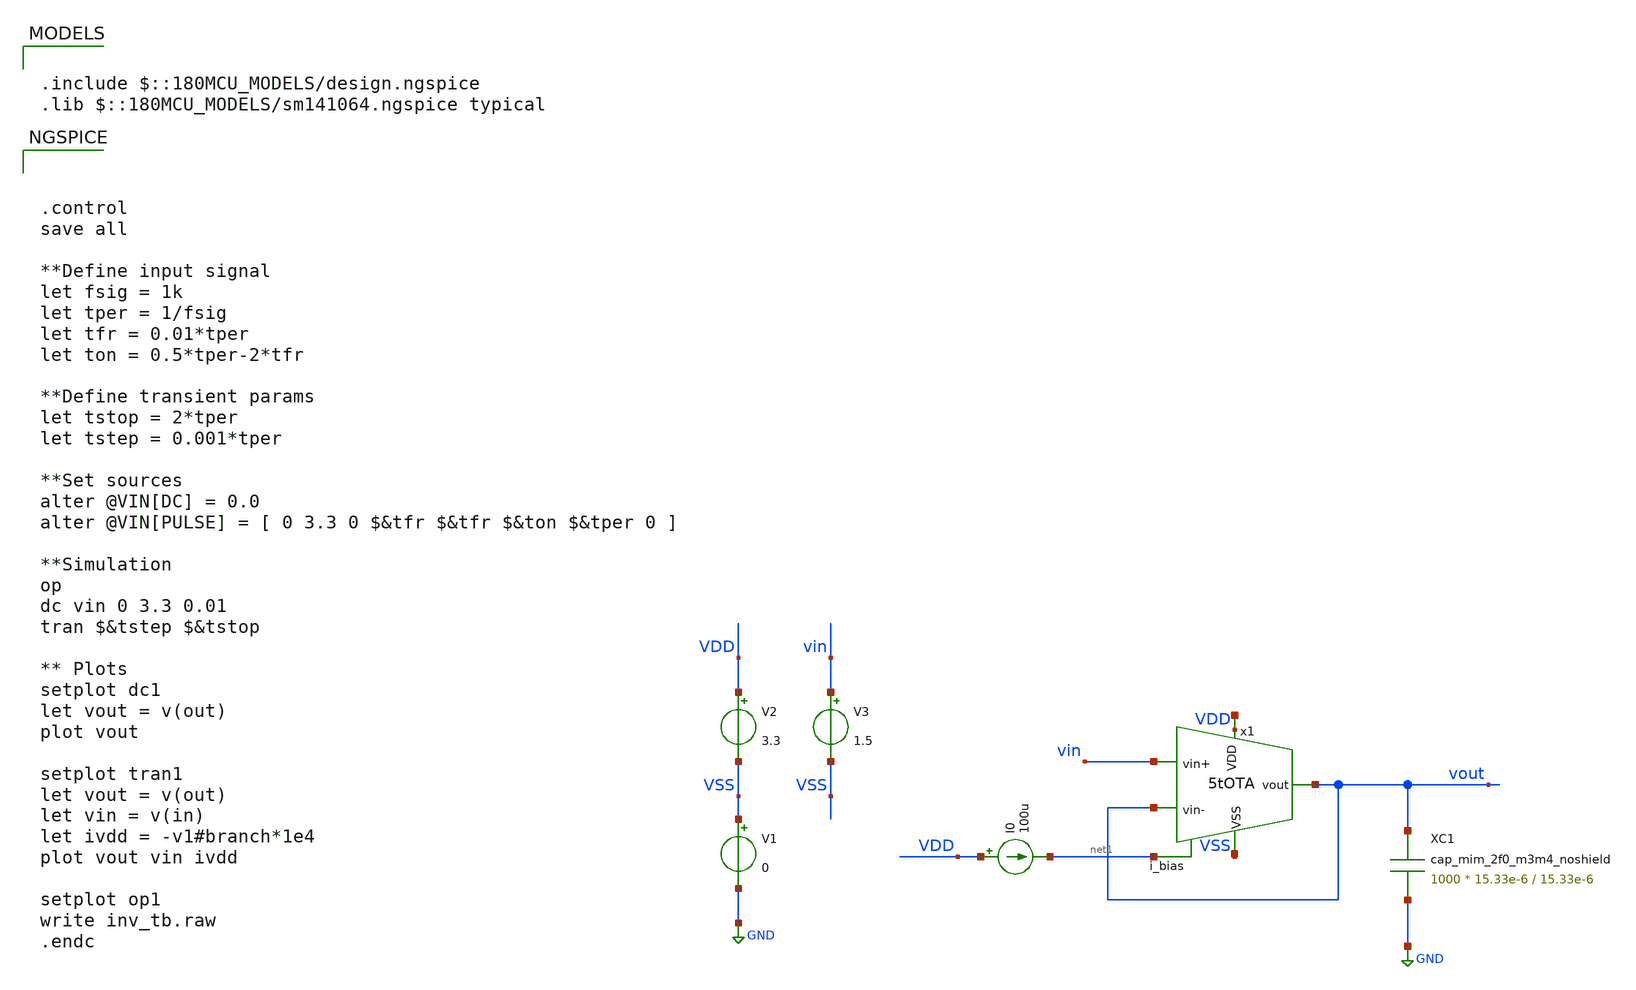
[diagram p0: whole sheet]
** sch_path: designs/5tOTA_tb.sch
**.subckt 5tOTA_tb
x1 net2 vout vin vout net1 net3 5tOTA
V1 VSS GND 0
V2 VDD VSS 3.3
I0 VDD net1 100u
V3 vin VSS 1.5
XC1 vout GND cap_mim_2f0_m3m4_noshield c_width=15.33e-6 c_length=15.33e-6 m=1000
**** begin user architecture code

.include $::180MCU_MODELS/design.ngspice
.lib $::180MCU_MODELS/sm141064.ngspice typical




.control
save all

**Define input signal
let fsig = 1k
let tper = 1/fsig
let tfr = 0.01*tper
let ton = 0.5*tper-2*tfr

**Define transient params
let tstop = 2*tper
let tstep = 0.001*tper

**Set sources
alter @VIN[DC] = 0.0
alter @VIN[PULSE] = [ 0 3.3 0 $&tfr $&tfr $&ton $&tper 0 ]

**Simulation
op
dc vin 0 3.3 0.01
tran $&tstep $&tstop

** Plots
setplot dc1
let vout = v(out)
plot vout

setplot tran1
let vout = v(out)
let vin = v(in)
let ivdd = -v1#branch*1e4
plot vout vin ivdd

setplot op1
write inv_tb.raw
.endc


**** end user architecture code
**.ends

* expanding   symbol:  5tOTA.sym # of pins=6
** sym_path: designs/5tOTA.sym
** sch_path: designs/5tOTA.sch
.subckt 5tOTA VDD vout vin+ vin- i_bias VSS
*.ipin VDD
*.opin vout
*.ipin i_bias
*.ipin vin+
*.ipin vin-
*.ipin VSS
XM1 net1 vin+ net2 VSS nfet_03v3 L=0.5u W=11.43u nf=1 ad='int((nf+1)/2) * W/nf * 0.18u' as='int((nf+2)/2) * W/nf * 0.18u'
+ pd='2*int((nf+1)/2) * (W/nf + 0.18u)' ps='2*int((nf+2)/2) * (W/nf + 0.18u)' nrd='0.18u / W' nrs='0.18u / W'
+ sa=0 sb=0 sd=0 m=1
XM2 vout vin- net2 VSS nfet_03v3 L=0.5u W=11.43u nf=1 ad='int((nf+1)/2) * W/nf * 0.18u' as='int((nf+2)/2) * W/nf * 0.18u'
+ pd='2*int((nf+1)/2) * (W/nf + 0.18u)' ps='2*int((nf+2)/2) * (W/nf + 0.18u)' nrd='0.18u / W' nrs='0.18u / W'
+ sa=0 sb=0 sd=0 m=1
XM3 net1 net1 VDD VDD pfet_03v3 L=0.5u W=22.86u nf=1 ad='int((nf+1)/2) * W/nf * 0.18u' as='int((nf+2)/2) * W/nf * 0.18u'
+ pd='2*int((nf+1)/2) * (W/nf + 0.18u)' ps='2*int((nf+2)/2) * (W/nf + 0.18u)' nrd='0.18u / W' nrs='0.18u / W'
+ sa=0 sb=0 sd=0 m=1
XM4 vout net1 VDD VDD pfet_03v3 L=0.5u W=22.86u nf=1 ad='int((nf+1)/2) * W/nf * 0.18u' as='int((nf+2)/2) * W/nf * 0.18u'
+ pd='2*int((nf+1)/2) * (W/nf + 0.18u)' ps='2*int((nf+2)/2) * (W/nf + 0.18u)' nrd='0.18u / W' nrs='0.18u / W'
+ sa=0 sb=0 sd=0 m=1
XM5 net2 i_bias VSS VSS nfet_03v3 L=0.5u W=22.86u nf=1 ad='int((nf+1)/2) * W/nf * 0.18u' as='int((nf+2)/2) * W/nf * 0.18u'
+ pd='2*int((nf+1)/2) * (W/nf + 0.18u)' ps='2*int((nf+2)/2) * (W/nf + 0.18u)' nrd='0.18u / W' nrs='0.18u / W'
+ sa=0 sb=0 sd=0 m=1
XM6 i_bias i_bias VSS VSS nfet_03v3 L=0.5u W=22.86u nf=1 ad='int((nf+1)/2) * W/nf * 0.18u' as='int((nf+2)/2) * W/nf * 0.18u'
+ pd='2*int((nf+1)/2) * (W/nf + 0.18u)' ps='2*int((nf+2)/2) * (W/nf + 0.18u)' nrd='0.18u / W' nrs='0.18u / W'
+ sa=0 sb=0 sd=0 m=1
.ends

.GLOBAL GND
.end
